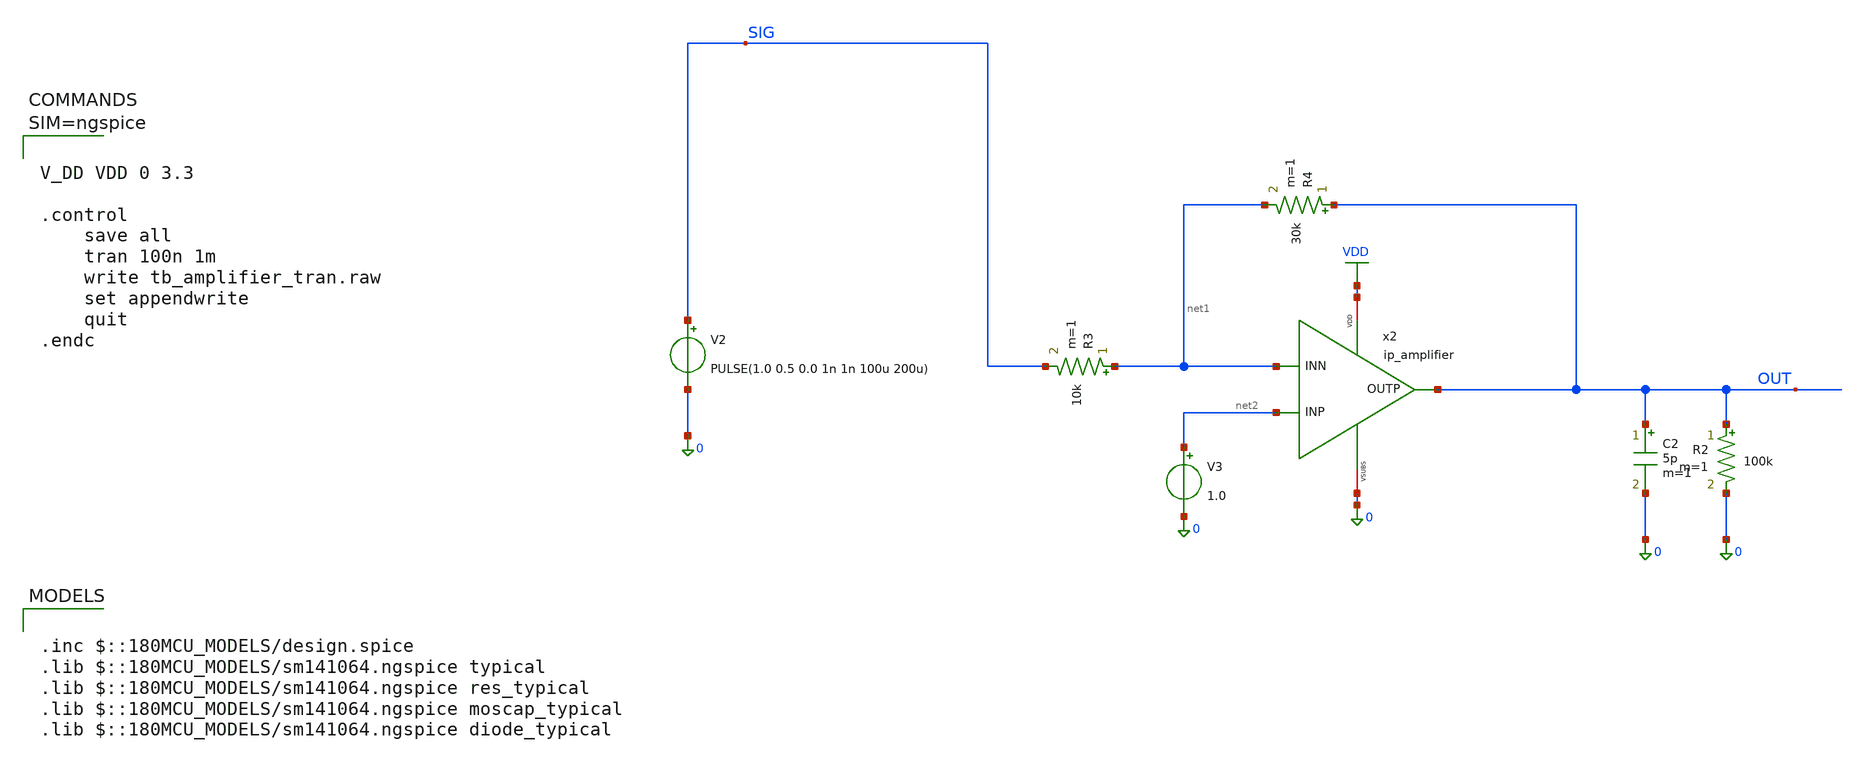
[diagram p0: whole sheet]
** sch_path: xschem/tb_amplifier_tran.sch
**.subckt tb_amplifier_tran
V2 SIG 0 PULSE(1.0 0.5 0.0 1n 1n 100u 200u)
x2 VDD OUT net2 net1 0 ip_amplifier
R2 OUT 0 100k m=1
C2 OUT 0 5p m=1
V3 net2 0 1.0
R3 net1 SIG 10k m=1
R4 OUT net1 30k m=1
**** begin user architecture code

.inc $::180MCU_MODELS/design.spice
.lib $::180MCU_MODELS/sm141064.ngspice typical
.lib $::180MCU_MODELS/sm141064.ngspice res_typical
.lib $::180MCU_MODELS/sm141064.ngspice moscap_typical
.lib $::180MCU_MODELS/sm141064.ngspice diode_typical




V_DD VDD 0 3.3

.control
	save all
	tran 100n 1m
	write tb_amplifier_tran.raw
	set appendwrite
	quit
.endc



**** end user architecture code
**.ends

* expanding   symbol:  ip_amplifier.sym # of pins=5
** sym_path: xschem/ip_amplifier.sym
** sch_path: xschem/ip_amplifier.sch
.subckt ip_amplifier VDD OUTP INP INN VSUBS
*.iopin VDD
*.iopin VSUBS
*.ipin INP
*.ipin INN
*.opin OUTP
XM1 net9 INP net7 VDD pfet_06v0 L=0.7u W=14u nf=1 ad='int((nf+1)/2) * W/nf * 0.18u' as='int((nf+2)/2) * W/nf * 0.18u'
+ pd='2*int((nf+1)/2) * (W/nf + 0.18u)' ps='2*int((nf+2)/2) * (W/nf + 0.18u)' nrd='0.18u / W' nrs='0.18u / W'
+ sa=0 sb=0 sd=0 m=1 par=1
XM2 net8 INN net7 VDD pfet_06v0 L=0.7u W=14u nf=1 ad='int((nf+1)/2) * W/nf * 0.18u' as='int((nf+2)/2) * W/nf * 0.18u'
+ pd='2*int((nf+1)/2) * (W/nf + 0.18u)' ps='2*int((nf+2)/2) * (W/nf + 0.18u)' nrd='0.18u / W' nrs='0.18u / W'
+ sa=0 sb=0 sd=0 m=1 par=1
XM5 net9 net1 VSUBS vsubs nfet_06v0 L=1u W=5u nf=1 ad='int((nf+1)/2) * W/nf * 0.18u' as='int((nf+2)/2) * W/nf * 0.18u'
+ pd='2*int((nf+1)/2) * (W/nf + 0.18u)' ps='2*int((nf+2)/2) * (W/nf + 0.18u)' nrd='0.18u / W' nrs='0.18u / W'
+ sa=0 sb=0 sd=0 m=1 par=1
XM6 net8 net1 VSUBS vsubs nfet_06v0 L=1u W=5u nf=1 ad='int((nf+1)/2) * W/nf * 0.18u' as='int((nf+2)/2) * W/nf * 0.18u'
+ pd='2*int((nf+1)/2) * (W/nf + 0.18u)' ps='2*int((nf+2)/2) * (W/nf + 0.18u)' nrd='0.18u / W' nrs='0.18u / W'
+ sa=0 sb=0 sd=0 m=1 par=1
XM3 net3 net1 VSUBS vsubs nfet_06v0 L=1u W=5u nf=1 ad='int((nf+1)/2) * W/nf * 0.18u' as='int((nf+2)/2) * W/nf * 0.18u'
+ pd='2*int((nf+1)/2) * (W/nf + 0.18u)' ps='2*int((nf+2)/2) * (W/nf + 0.18u)' nrd='0.18u / W' nrs='0.18u / W'
+ sa=0 sb=0 sd=0 m=1 par=1
XM4 net2 net1 VSUBS vsubs nfet_06v0 L=1u W=5u nf=1 ad='int((nf+1)/2) * W/nf * 0.18u' as='int((nf+2)/2) * W/nf * 0.18u'
+ pd='2*int((nf+1)/2) * (W/nf + 0.18u)' ps='2*int((nf+2)/2) * (W/nf + 0.18u)' nrd='0.18u / W' nrs='0.18u / W'
+ sa=0 sb=0 sd=0 m=1 par=1
XM7 net1 net1 net3 vsubs nfet_06v0 L=0.7u W=35u nf=1 ad='int((nf+1)/2) * W/nf * 0.18u' as='int((nf+2)/2) * W/nf * 0.18u'
+ pd='2*int((nf+1)/2) * (W/nf + 0.18u)' ps='2*int((nf+2)/2) * (W/nf + 0.18u)' nrd='0.18u / W' nrs='0.18u / W'
+ sa=0 sb=0 sd=0 m=1 par=1
XM8 net4 net1 net2 vsubs nfet_06v0 L=0.7u W=35u nf=1 ad='int((nf+1)/2) * W/nf * 0.18u' as='int((nf+2)/2) * W/nf * 0.18u'
+ pd='2*int((nf+1)/2) * (W/nf + 0.18u)' ps='2*int((nf+2)/2) * (W/nf + 0.18u)' nrd='0.18u / W' nrs='0.18u / W'
+ sa=0 sb=0 sd=0 m=1 par=1
I0 VDD net1 20u
XM9 net5 net4 VDD VDD pfet_06v0 L=1u W=6u nf=1 ad='int((nf+1)/2) * W/nf * 0.18u' as='int((nf+2)/2) * W/nf * 0.18u'
+ pd='2*int((nf+1)/2) * (W/nf + 0.18u)' ps='2*int((nf+2)/2) * (W/nf + 0.18u)' nrd='0.18u / W' nrs='0.18u / W'
+ sa=0 sb=0 sd=0 m=1 par=1
XM10 net6 net4 VDD VDD pfet_06v0 L=1u W=6u nf=1 ad='int((nf+1)/2) * W/nf * 0.18u' as='int((nf+2)/2) * W/nf * 0.18u'
+ pd='2*int((nf+1)/2) * (W/nf + 0.18u)' ps='2*int((nf+2)/2) * (W/nf + 0.18u)' nrd='0.18u / W' nrs='0.18u / W'
+ sa=0 sb=0 sd=0 m=1 par=1
XM11 net4 net4 net5 VDD pfet_06v0 L=0.7u W=35u nf=1 ad='int((nf+1)/2) * W/nf * 0.18u' as='int((nf+2)/2) * W/nf * 0.18u'
+ pd='2*int((nf+1)/2) * (W/nf + 0.18u)' ps='2*int((nf+2)/2) * (W/nf + 0.18u)' nrd='0.18u / W' nrs='0.18u / W'
+ sa=0 sb=0 sd=0 m=1 par=1
XM12 net7 net4 net6 VDD pfet_06v0 L=0.7u W=35u nf=1 ad='int((nf+1)/2) * W/nf * 0.18u' as='int((nf+2)/2) * W/nf * 0.18u'
+ pd='2*int((nf+1)/2) * (W/nf + 0.18u)' ps='2*int((nf+2)/2) * (W/nf + 0.18u)' nrd='0.18u / W' nrs='0.18u / W'
+ sa=0 sb=0 sd=0 m=1 par=1
XM13 net10 net1 net8 vsubs nfet_06v0 L=0.7u W=35u nf=1 ad='int((nf+1)/2) * W/nf * 0.18u' as='int((nf+2)/2) * W/nf * 0.18u'
+ pd='2*int((nf+1)/2) * (W/nf + 0.18u)' ps='2*int((nf+2)/2) * (W/nf + 0.18u)' nrd='0.18u / W' nrs='0.18u / W'
+ sa=0 sb=0 sd=0 m=1 par=1
XM14 net11 net1 net9 vsubs nfet_06v0 L=0.7u W=35u nf=1 ad='int((nf+1)/2) * W/nf * 0.18u' as='int((nf+2)/2) * W/nf * 0.18u'
+ pd='2*int((nf+1)/2) * (W/nf + 0.18u)' ps='2*int((nf+2)/2) * (W/nf + 0.18u)' nrd='0.18u / W' nrs='0.18u / W'
+ sa=0 sb=0 sd=0 m=1 par=1
XM15 net10 net10 VDD VDD pfet_06v0 L=0.7u W=14u nf=1 ad='int((nf+1)/2) * W/nf * 0.18u' as='int((nf+2)/2) * W/nf * 0.18u'
+ pd='2*int((nf+1)/2) * (W/nf + 0.18u)' ps='2*int((nf+2)/2) * (W/nf + 0.18u)' nrd='0.18u / W' nrs='0.18u / W'
+ sa=0 sb=0 sd=0 m=1 par=1
XM16 net11 net10 VDD VDD pfet_06v0 L=0.7u W=14u nf=1 ad='int((nf+1)/2) * W/nf * 0.18u' as='int((nf+2)/2) * W/nf * 0.18u'
+ pd='2*int((nf+1)/2) * (W/nf + 0.18u)' ps='2*int((nf+2)/2) * (W/nf + 0.18u)' nrd='0.18u / W' nrs='0.18u / W'
+ sa=0 sb=0 sd=0 m=1 par=1
XM17 OUTP net11 VDD VDD pfet_06v0 L=0.5u W=30u nf=1 ad='int((nf+1)/2) * W/nf * 0.18u' as='int((nf+2)/2) * W/nf * 0.18u'
+ pd='2*int((nf+1)/2) * (W/nf + 0.18u)' ps='2*int((nf+2)/2) * (W/nf + 0.18u)' nrd='0.18u / W' nrs='0.18u / W'
+ sa=0 sb=0 sd=0 m=1 par=1
XM18 OUTP net9 VSUBS vsubs nfet_06v0 L=5u W=10u nf=1 ad='int((nf+1)/2) * W/nf * 0.18u' as='int((nf+2)/2) * W/nf * 0.18u'
+ pd='2*int((nf+1)/2) * (W/nf + 0.18u)' ps='2*int((nf+2)/2) * (W/nf + 0.18u)' nrd='0.18u / W' nrs='0.18u / W'
+ sa=0 sb=0 sd=0 m=1 par=1
C1 OUTP net11 5p m=1
.ends

.GLOBAL VDD
.end
